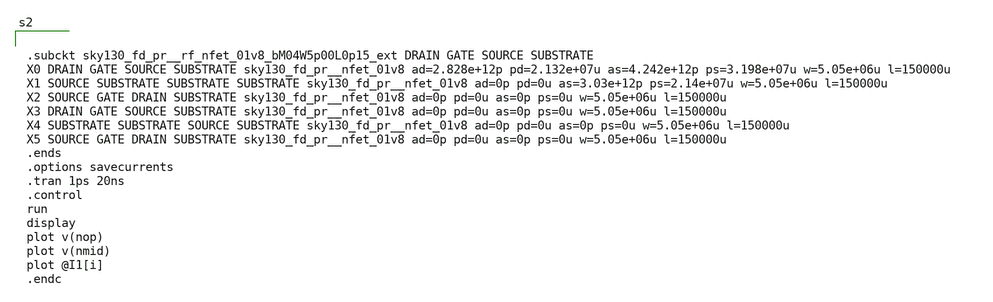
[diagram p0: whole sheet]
** sch_path: xschem/untitled-8.sch
**.subckt untitled-8
**** begin user architecture code
.lib $::SKYWATER_MODELS/sky130.lib.spice ff
* .include $::PDKPATH/libs.ref/sky130_fd_sc_hvl/spice/sky130_fd_sc_hvl.spice



.subckt sky130_fd_pr__rf_nfet_01v8_bM04W5p00L0p15_ext DRAIN GATE SOURCE SUBSTRATE
X0 DRAIN GATE SOURCE SUBSTRATE sky130_fd_pr__nfet_01v8 ad=2.828e+12p pd=2.132e+07u as=4.242e+12p
+ ps=3.198e+07u w=5.05e+06u l=150000u
X1 SOURCE SUBSTRATE SUBSTRATE SUBSTRATE sky130_fd_pr__nfet_01v8 ad=0p pd=0u as=3.03e+12p
+ ps=2.14e+07u w=5.05e+06u l=150000u
X2 SOURCE GATE DRAIN SUBSTRATE sky130_fd_pr__nfet_01v8 ad=0p pd=0u as=0p ps=0u w=5.05e+06u l=150000u
X3 DRAIN GATE SOURCE SUBSTRATE sky130_fd_pr__nfet_01v8 ad=0p pd=0u as=0p ps=0u w=5.05e+06u l=150000u
X4 SUBSTRATE SUBSTRATE SOURCE SUBSTRATE sky130_fd_pr__nfet_01v8 ad=0p pd=0u as=0p ps=0u w=5.05e+06u
+ l=150000u
X5 SOURCE GATE DRAIN SUBSTRATE sky130_fd_pr__nfet_01v8 ad=0p pd=0u as=0p ps=0u w=5.05e+06u l=150000u
.ends
.options savecurrents
.tran 1ps 20ns
.control
run
display
plot v(nop)
plot v(nmid)
plot @I1[i]
.endc


**** end user architecture code
**.ends
.end
